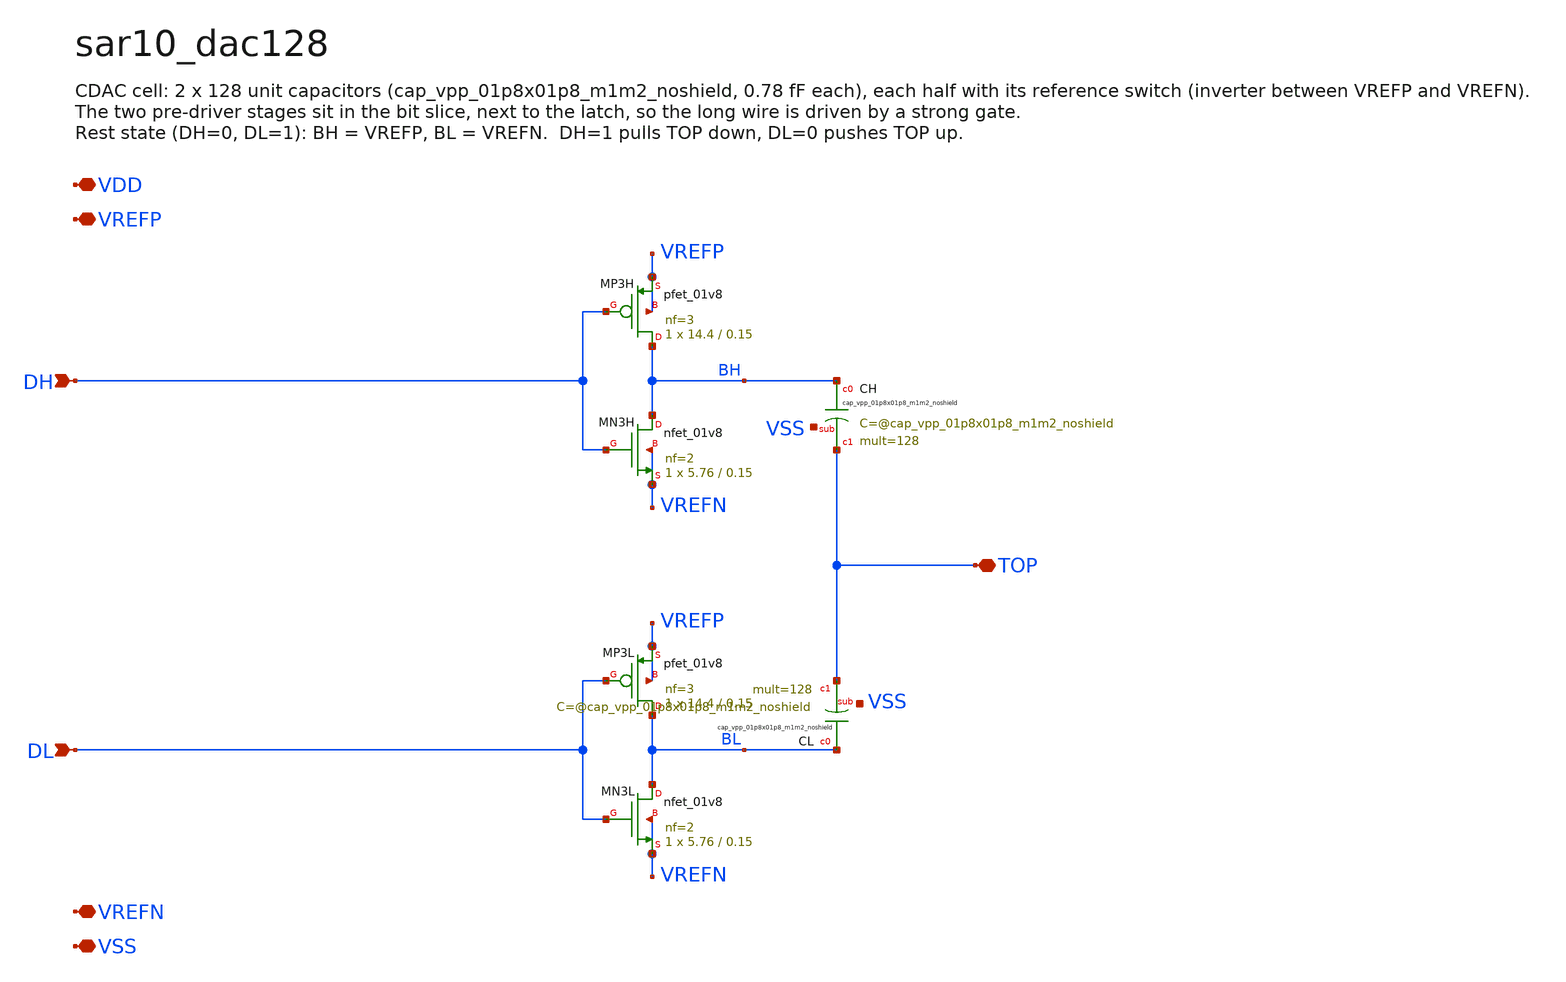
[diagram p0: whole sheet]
** sch_path: xschem/sar10_dac128.sch
**.subckt sar10_dac128 DH DL TOP VDD VREFP VREFN VSS
*.ipin DH
*.ipin DL
*.iopin TOP
*.iopin VDD
*.iopin VREFP
*.iopin VREFN
*.iopin VSS
XMP3H BH DH VREFP VREFP sky130_fd_pr__pfet_01v8 L=0.15 W=14.4 nf=3 ad='int((3 + 1)/2) * 14.4 / 3 * 0.29'
+ as='int((3 + 2)/2) * 14.4 / 3 * 0.29' pd='2*int((3 + 1)/2) * (14.4 / 3 + 0.29)' ps='2*int((3 + 2)/2) * (14.4 / 3 + 0.29)'
+ nrd='0.29 / 14.4 ' nrs='0.29 / 14.4 ' sa=0 sb=0 sd=0 mult=1 m=1
XMN3H BH DH VREFN VREFN sky130_fd_pr__nfet_01v8 L=0.15 W=5.76 nf=2 ad='int((2 + 1)/2) * 5.76 / 2 * 0.29'
+ as='int((2 + 2)/2) * 5.76 / 2 * 0.29' pd='2*int((2 + 1)/2) * (5.76 / 2 + 0.29)' ps='2*int((2 + 2)/2) * (5.76 / 2 + 0.29)'
+ nrd='0.29 / 5.76 ' nrs='0.29 / 5.76 ' sa=0 sb=0 sd=0 mult=1 m=1
XMP3L BL DL VREFP VREFP sky130_fd_pr__pfet_01v8 L=0.15 W=14.4 nf=3 ad='int((3 + 1)/2) * 14.4 / 3 * 0.29'
+ as='int((3 + 2)/2) * 14.4 / 3 * 0.29' pd='2*int((3 + 1)/2) * (14.4 / 3 + 0.29)' ps='2*int((3 + 2)/2) * (14.4 / 3 + 0.29)'
+ nrd='0.29 / 14.4 ' nrs='0.29 / 14.4 ' sa=0 sb=0 sd=0 mult=1 m=1
XMN3L BL DL VREFN VREFN sky130_fd_pr__nfet_01v8 L=0.15 W=5.76 nf=2 ad='int((2 + 1)/2) * 5.76 / 2 * 0.29'
+ as='int((2 + 2)/2) * 5.76 / 2 * 0.29' pd='2*int((2 + 1)/2) * (5.76 / 2 + 0.29)' ps='2*int((2 + 2)/2) * (5.76 / 2 + 0.29)'
+ nrd='0.29 / 5.76 ' nrs='0.29 / 5.76 ' sa=0 sb=0 sd=0 mult=1 m=1
XCH BH TOP VSS sky130_fd_pr__cap_vpp_01p8x01p8_m1m2_noshield mult=128 m=128
XCL BL TOP VSS sky130_fd_pr__cap_vpp_01p8x01p8_m1m2_noshield mult=128 m=128
**.ends
.end
